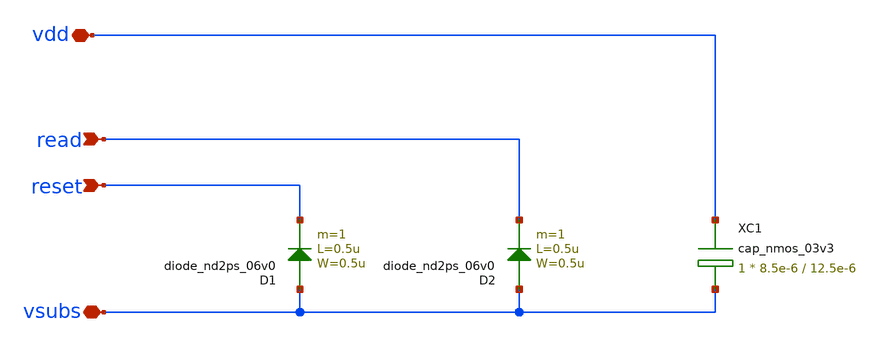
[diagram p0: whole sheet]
** sch_path: xschem/ip_pixel_frame_right.sch
**.subckt ip_pixel_frame_right read reset vsubs vdd
*.ipin read
*.ipin reset
*.iopin vsubs
*.iopin vdd
D1 vsubs reset diode_nd2ps_06v0 area='0.5u * 0.5u ' pj='2*0.5u + 2*0.5u ' m=1
D2 vsubs read diode_nd2ps_06v0 area='0.5u * 0.5u ' pj='2*0.5u + 2*0.5u ' m=1
XC1 vdd vsubs cap_nmos_03v3 c_width=8.5e-6 c_length=12.5e-6 m=1
**.ends
.end
